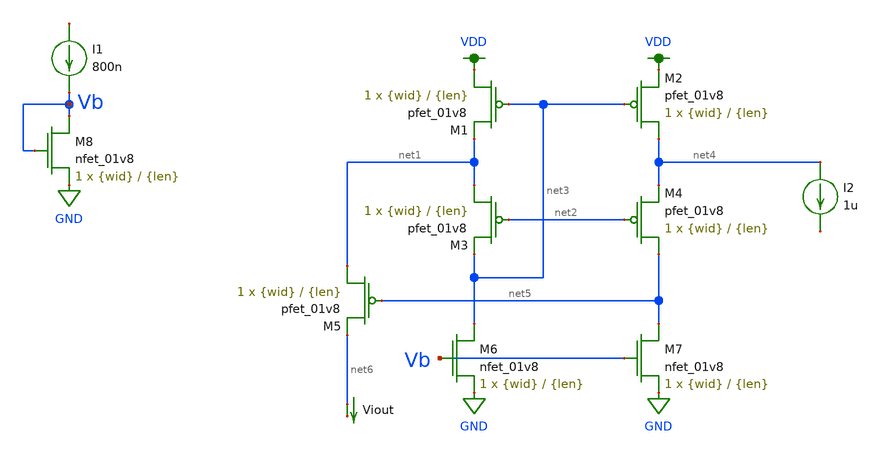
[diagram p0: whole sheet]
** sch_path: mp3/untitled.sch
**.subckt untitled
XM1 VDD net3 net1 VDD sky130_fd_pr__pfet_01v8 L={len} W={wid} nf=1 ad='int((nf+1)/2) * W/nf * 0.29' as='int((nf+2)/2) * W/nf * 0.29'
+ pd='2*int((nf+1)/2) * (W/nf + 0.29)' ps='2*int((nf+2)/2) * (W/nf + 0.29)' nrd='0.29 / W' nrs='0.29 / W'
+ sa=0 sb=0 sd=0 mult=1 m=1
XM2 net4 net3 VDD VDD sky130_fd_pr__pfet_01v8 L={len} W={wid} nf=1 ad='int((nf+1)/2) * W/nf * 0.29' as='int((nf+2)/2) * W/nf * 0.29'
+ pd='2*int((nf+1)/2) * (W/nf + 0.29)' ps='2*int((nf+2)/2) * (W/nf + 0.29)' nrd='0.29 / W' nrs='0.29 / W'
+ sa=0 sb=0 sd=0 mult=1 m=1
XM3 net1 net2 net3 VDD sky130_fd_pr__pfet_01v8 L={len} W={wid} nf=1 ad='int((nf+1)/2) * W/nf * 0.29'
+ as='int((nf+2)/2) * W/nf * 0.29' pd='2*int((nf+1)/2) * (W/nf + 0.29)' ps='2*int((nf+2)/2) * (W/nf + 0.29)'
+ nrd='0.29 / W' nrs='0.29 / W' sa=0 sb=0 sd=0 mult=1 m=1
XM4 net5 net2 net4 VDD sky130_fd_pr__pfet_01v8 L={len} W={wid} nf=1 ad='int((nf+1)/2) * W/nf * 0.29'
+ as='int((nf+2)/2) * W/nf * 0.29' pd='2*int((nf+1)/2) * (W/nf + 0.29)' ps='2*int((nf+2)/2) * (W/nf + 0.29)'
+ nrd='0.29 / W' nrs='0.29 / W' sa=0 sb=0 sd=0 mult=1 m=1
XM5 net1 net5 net6 VDD sky130_fd_pr__pfet_01v8 L={len} W={wid} nf=1 ad='int((nf+1)/2) * W/nf * 0.29'
+ as='int((nf+2)/2) * W/nf * 0.29' pd='2*int((nf+1)/2) * (W/nf + 0.29)' ps='2*int((nf+2)/2) * (W/nf + 0.29)'
+ nrd='0.29 / W' nrs='0.29 / W' sa=0 sb=0 sd=0 mult=1 m=1
XM6 net3 Vb GND GND sky130_fd_pr__nfet_01v8 L={len} W={wid} nf=1 ad='int((nf+1)/2) * W/nf * 0.29' as='int((nf+2)/2) * W/nf * 0.29'
+ pd='2*int((nf+1)/2) * (W/nf + 0.29)' ps='2*int((nf+2)/2) * (W/nf + 0.29)' nrd='0.29 / W' nrs='0.29 / W'
+ sa=0 sb=0 sd=0 mult=1 m=1
XM7 net5 Vb GND GND sky130_fd_pr__nfet_01v8 L={len} W={wid} nf=1 ad='int((nf+1)/2) * W/nf * 0.29' as='int((nf+2)/2) * W/nf * 0.29'
+ pd='2*int((nf+1)/2) * (W/nf + 0.29)' ps='2*int((nf+2)/2) * (W/nf + 0.29)' nrd='0.29 / W' nrs='0.29 / W'
+ sa=0 sb=0 sd=0 mult=1 m=1
XM8 Vb Vb GND GND sky130_fd_pr__nfet_01v8 L={len} W={wid} nf=1 ad='int((nf+1)/2) * W/nf * 0.29' as='int((nf+2)/2) * W/nf * 0.29'
+ pd='2*int((nf+1)/2) * (W/nf + 0.29)' ps='2*int((nf+2)/2) * (W/nf + 0.29)' nrd='0.29 / W' nrs='0.29 / W'
+ sa=0 sb=0 sd=0 mult=1 m=1
I1 net7 Vb 800n
I2 net4 net8 1u
Viout net6 net9 0
.save i(viout)
**.ends
.GLOBAL GND
.GLOBAL VDD
.end
